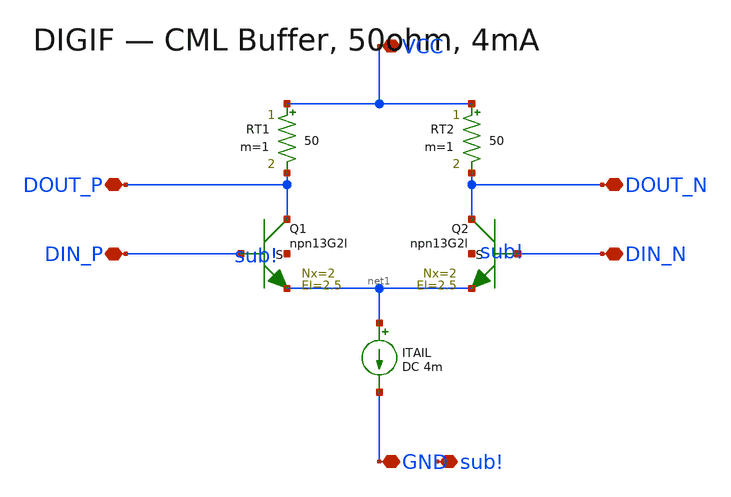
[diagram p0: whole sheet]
** sch_path: xschem/blocks/DIGIF_CML.sch
**.subckt DIGIF_CML DIN_P DIN_N DOUT_P DOUT_N VCC GND sub!
*.iopin DIN_P
*.iopin DIN_N
*.iopin DOUT_P
*.iopin DOUT_N
*.iopin VCC
*.iopin GND
*.iopin sub!
XQ1 DOUT_P DIN_P net1 sub! npn13G2l Nx=2 El=2.5 mm_ok=1
XQ2 DOUT_N DIN_N net1 sub! npn13G2l Nx=2 El=2.5 mm_ok=1
RT1 VCC DOUT_P 50 m=1
RT2 VCC DOUT_N 50 m=1
ITAIL net1 GND DC 4m
**.ends
.end
